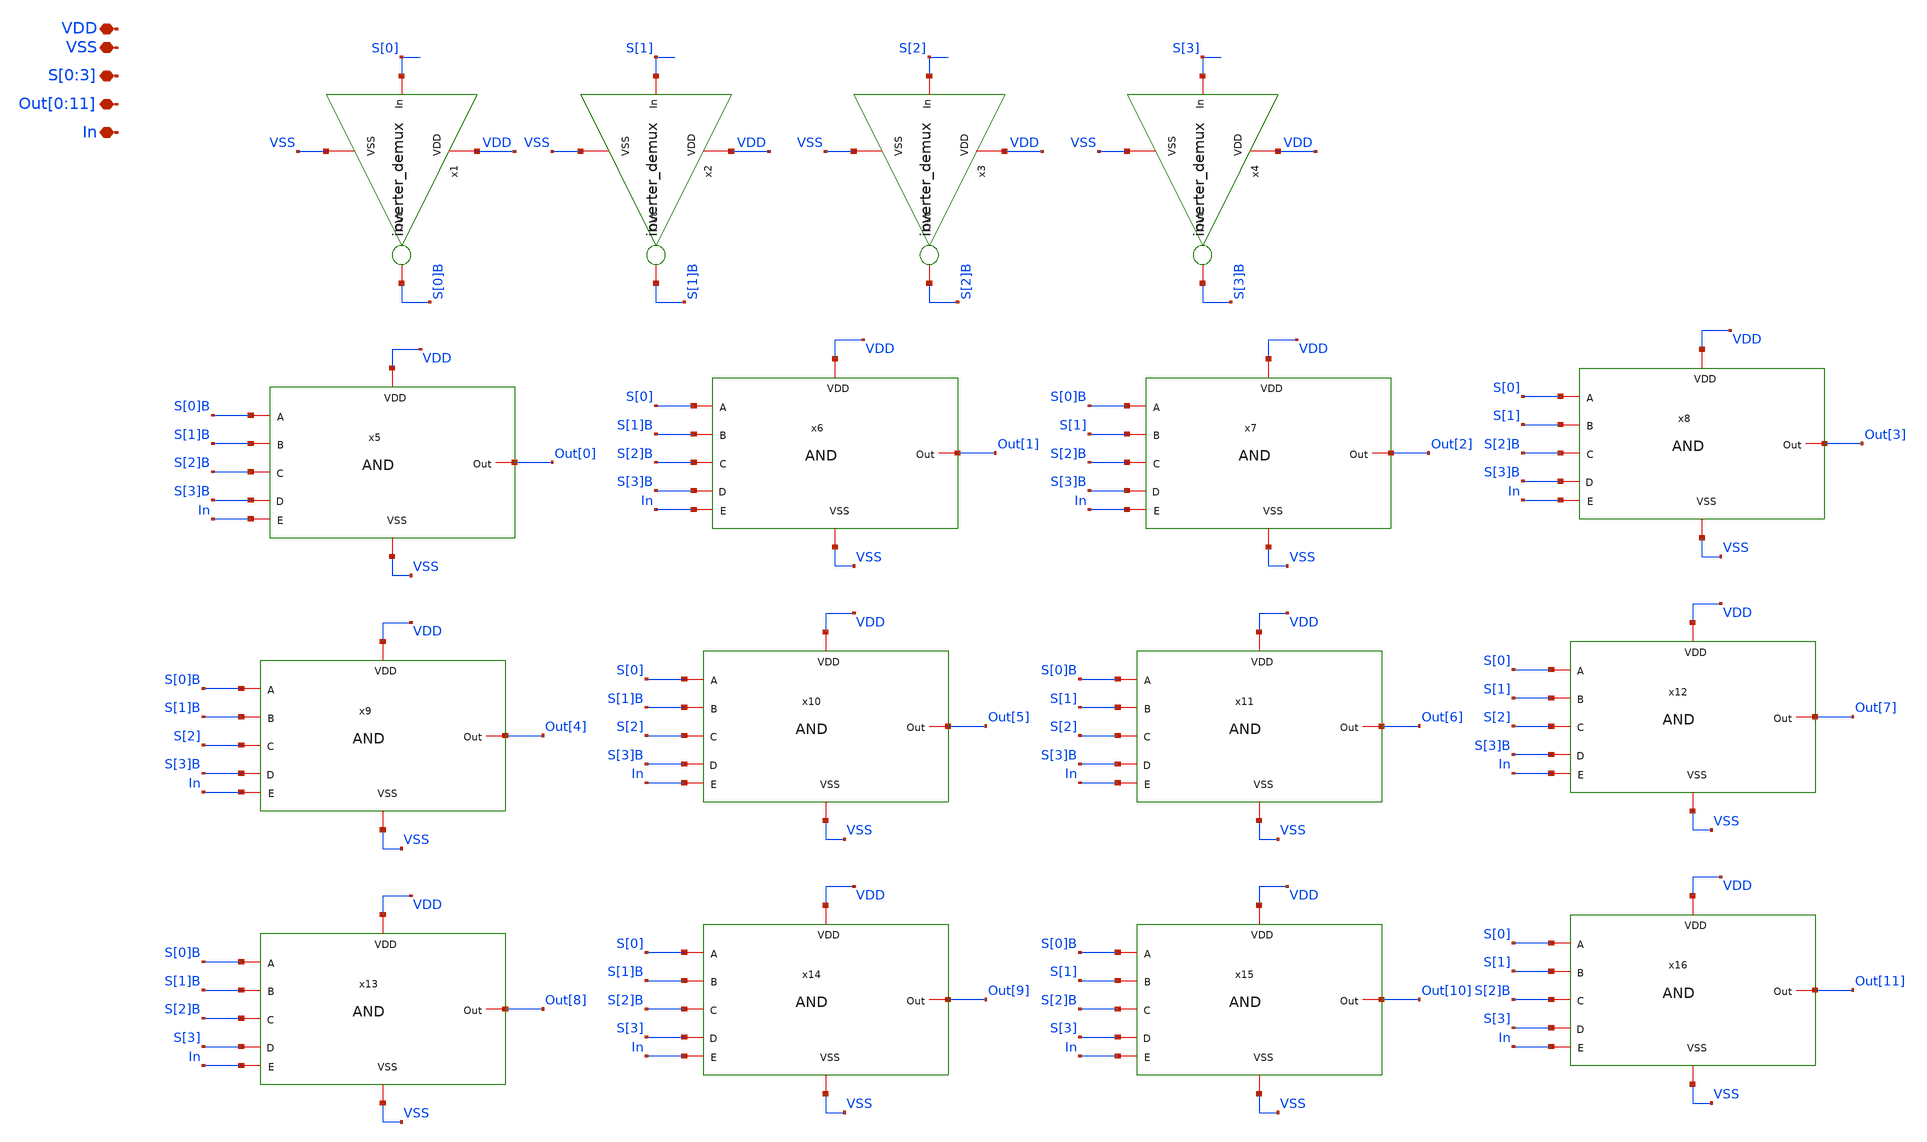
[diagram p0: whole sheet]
** sch_path: MUX/Demux.sch
**.subckt Demux S[0],S[1],S[2],S[3] VSS VDD
*+ Out[0],Out[1],Out[2],Out[3],Out[4],Out[5],Out[6],Out[7],Out[8],Out[9],Out[10],Out[11] In
*.iopin S[0],S[1],S[2],S[3]
*.iopin VSS
*.iopin VDD
*.iopin Out[0],Out[1],Out[2],Out[3],Out[4],Out[5],Out[6],Out[7],Out[8],Out[9],Out[10],Out[11]
*.iopin In
x5 VDD In S[0]B S[1]B S[2]B S[3]B Out[0] VSS AND
x6 VDD In S[0] S[1]B S[2]B S[3]B Out[1] VSS AND
x7 VDD In S[0]B S[1] S[2]B S[3]B Out[2] VSS AND
x8 VDD In S[0] S[1] S[2]B S[3]B Out[3] VSS AND
x9 VDD In S[0]B S[1]B S[2] S[3]B Out[4] VSS AND
x10 VDD In S[0] S[1]B S[2] S[3]B Out[5] VSS AND
x11 VDD In S[0]B S[1] S[2] S[3]B Out[6] VSS AND
x12 VDD In S[0] S[1] S[2] S[3]B Out[7] VSS AND
x13 VDD In S[0]B S[1]B S[2]B S[3] Out[8] VSS AND
x14 VDD In S[0] S[1]B S[2]B S[3] Out[9] VSS AND
x15 VDD In S[0]B S[1] S[2]B S[3] Out[10] VSS AND
x16 VDD In S[0] S[1] S[2]B S[3] Out[11] VSS AND
x1 VDD S[0]B S[0] VSS inverter_demux
x2 VDD S[1]B S[1] VSS inverter_demux
x3 VDD S[2]B S[2] VSS inverter_demux
x4 VDD S[3]B S[3] VSS inverter_demux
**.ends

* expanding   symbol:  AND.sym # of pins=8
** sym_path: MUX/AND.sym
** sch_path: MUX/AND.sch
.subckt AND VDD E A B C D Out VSS
*.iopin VDD
*.iopin A
*.iopin VSS
*.iopin B
*.iopin Out
*.iopin C
*.iopin D
*.iopin E
XM3 net1 A net2 VSS sky130_fd_pr__nfet_01v8 L=0.15 W=0.65 nf=1 ad='int((nf+1)/2) * W/nf * 0.29' as='int((nf+2)/2) * W/nf * 0.29'
+ pd='2*int((nf+1)/2) * (W/nf + 0.29)' ps='2*int((nf+2)/2) * (W/nf + 0.29)' nrd='0.29 / W' nrs='0.29 / W'
+ sa=0 sb=0 sd=0 mult=1 m=1
XM1 net1 A VDD VDD sky130_fd_pr__pfet_01v8 L=0.15 W=1 nf=1 ad='int((nf+1)/2) * W/nf * 0.29' as='int((nf+2)/2) * W/nf * 0.29'
+ pd='2*int((nf+1)/2) * (W/nf + 0.29)' ps='2*int((nf+2)/2) * (W/nf + 0.29)' nrd='0.29 / W' nrs='0.29 / W'
+ sa=0 sb=0 sd=0 mult=1 m=1
XM5 Out net1 VSS VSS sky130_fd_pr__nfet_01v8 L=0.15 W=0.65 nf=1 ad='int((nf+1)/2) * W/nf * 0.29' as='int((nf+2)/2) * W/nf * 0.29'
+ pd='2*int((nf+1)/2) * (W/nf + 0.29)' ps='2*int((nf+2)/2) * (W/nf + 0.29)' nrd='0.29 / W' nrs='0.29 / W'
+ sa=0 sb=0 sd=0 mult=1 m=1
XM6 Out net1 VDD VDD sky130_fd_pr__pfet_01v8 L=0.15 W=1 nf=1 ad='int((nf+1)/2) * W/nf * 0.29' as='int((nf+2)/2) * W/nf * 0.29'
+ pd='2*int((nf+1)/2) * (W/nf + 0.29)' ps='2*int((nf+2)/2) * (W/nf + 0.29)' nrd='0.29 / W' nrs='0.29 / W'
+ sa=0 sb=0 sd=0 mult=1 m=1
XM4 net1 B VDD VDD sky130_fd_pr__pfet_01v8 L=0.15 W=1 nf=1 ad='int((nf+1)/2) * W/nf * 0.29' as='int((nf+2)/2) * W/nf * 0.29'
+ pd='2*int((nf+1)/2) * (W/nf + 0.29)' ps='2*int((nf+2)/2) * (W/nf + 0.29)' nrd='0.29 / W' nrs='0.29 / W'
+ sa=0 sb=0 sd=0 mult=1 m=1
XM10 net1 C VDD VDD sky130_fd_pr__pfet_01v8 L=0.15 W=1 nf=1 ad='int((nf+1)/2) * W/nf * 0.29' as='int((nf+2)/2) * W/nf * 0.29'
+ pd='2*int((nf+1)/2) * (W/nf + 0.29)' ps='2*int((nf+2)/2) * (W/nf + 0.29)' nrd='0.29 / W' nrs='0.29 / W'
+ sa=0 sb=0 sd=0 mult=1 m=1
XM11 net1 D VDD VDD sky130_fd_pr__pfet_01v8 L=0.15 W=1 nf=1 ad='int((nf+1)/2) * W/nf * 0.29' as='int((nf+2)/2) * W/nf * 0.29'
+ pd='2*int((nf+1)/2) * (W/nf + 0.29)' ps='2*int((nf+2)/2) * (W/nf + 0.29)' nrd='0.29 / W' nrs='0.29 / W'
+ sa=0 sb=0 sd=0 mult=1 m=1
XM12 net1 E VDD VDD sky130_fd_pr__pfet_01v8 L=0.15 W=1 nf=1 ad='int((nf+1)/2) * W/nf * 0.29' as='int((nf+2)/2) * W/nf * 0.29'
+ pd='2*int((nf+1)/2) * (W/nf + 0.29)' ps='2*int((nf+2)/2) * (W/nf + 0.29)' nrd='0.29 / W' nrs='0.29 / W'
+ sa=0 sb=0 sd=0 mult=1 m=1
XM2 net2 B net5 VSS sky130_fd_pr__nfet_01v8 L=0.15 W=0.65 nf=1 ad='int((nf+1)/2) * W/nf * 0.29' as='int((nf+2)/2) * W/nf * 0.29'
+ pd='2*int((nf+1)/2) * (W/nf + 0.29)' ps='2*int((nf+2)/2) * (W/nf + 0.29)' nrd='0.29 / W' nrs='0.29 / W'
+ sa=0 sb=0 sd=0 mult=1 m=1
XM7 net5 C net4 VSS sky130_fd_pr__nfet_01v8 L=0.15 W=0.65 nf=1 ad='int((nf+1)/2) * W/nf * 0.29' as='int((nf+2)/2) * W/nf * 0.29'
+ pd='2*int((nf+1)/2) * (W/nf + 0.29)' ps='2*int((nf+2)/2) * (W/nf + 0.29)' nrd='0.29 / W' nrs='0.29 / W'
+ sa=0 sb=0 sd=0 mult=1 m=1
XM8 net4 D net3 VSS sky130_fd_pr__nfet_01v8 L=0.15 W=0.65 nf=1 ad='int((nf+1)/2) * W/nf * 0.29' as='int((nf+2)/2) * W/nf * 0.29'
+ pd='2*int((nf+1)/2) * (W/nf + 0.29)' ps='2*int((nf+2)/2) * (W/nf + 0.29)' nrd='0.29 / W' nrs='0.29 / W'
+ sa=0 sb=0 sd=0 mult=1 m=1
XM9 net3 E VSS VSS sky130_fd_pr__nfet_01v8 L=0.15 W=0.65 nf=1 ad='int((nf+1)/2) * W/nf * 0.29' as='int((nf+2)/2) * W/nf * 0.29'
+ pd='2*int((nf+1)/2) * (W/nf + 0.29)' ps='2*int((nf+2)/2) * (W/nf + 0.29)' nrd='0.29 / W' nrs='0.29 / W'
+ sa=0 sb=0 sd=0 mult=1 m=1
.ends


* expanding   symbol:  inverter_demux.sym # of pins=4
** sym_path: MUX/inverter_demux.sym
** sch_path: MUX/inverter_demux.sch
.subckt inverter_demux VDD Out In VSS
*.iopin VDD
*.iopin Out
*.iopin VSS
*.iopin In
XM3 Out In VSS VSS sky130_fd_pr__nfet_01v8 L=0.15 W=0.65 nf=1 ad='int((nf+1)/2) * W/nf * 0.29' as='int((nf+2)/2) * W/nf * 0.29'
+ pd='2*int((nf+1)/2) * (W/nf + 0.29)' ps='2*int((nf+2)/2) * (W/nf + 0.29)' nrd='0.29 / W' nrs='0.29 / W'
+ sa=0 sb=0 sd=0 mult=1 m=1
XM1 Out In VDD VDD sky130_fd_pr__pfet_01v8 L=0.15 W=1 nf=1 ad='int((nf+1)/2) * W/nf * 0.29' as='int((nf+2)/2) * W/nf * 0.29'
+ pd='2*int((nf+1)/2) * (W/nf + 0.29)' ps='2*int((nf+2)/2) * (W/nf + 0.29)' nrd='0.29 / W' nrs='0.29 / W'
+ sa=0 sb=0 sd=0 mult=1 m=1
.ends

.end
